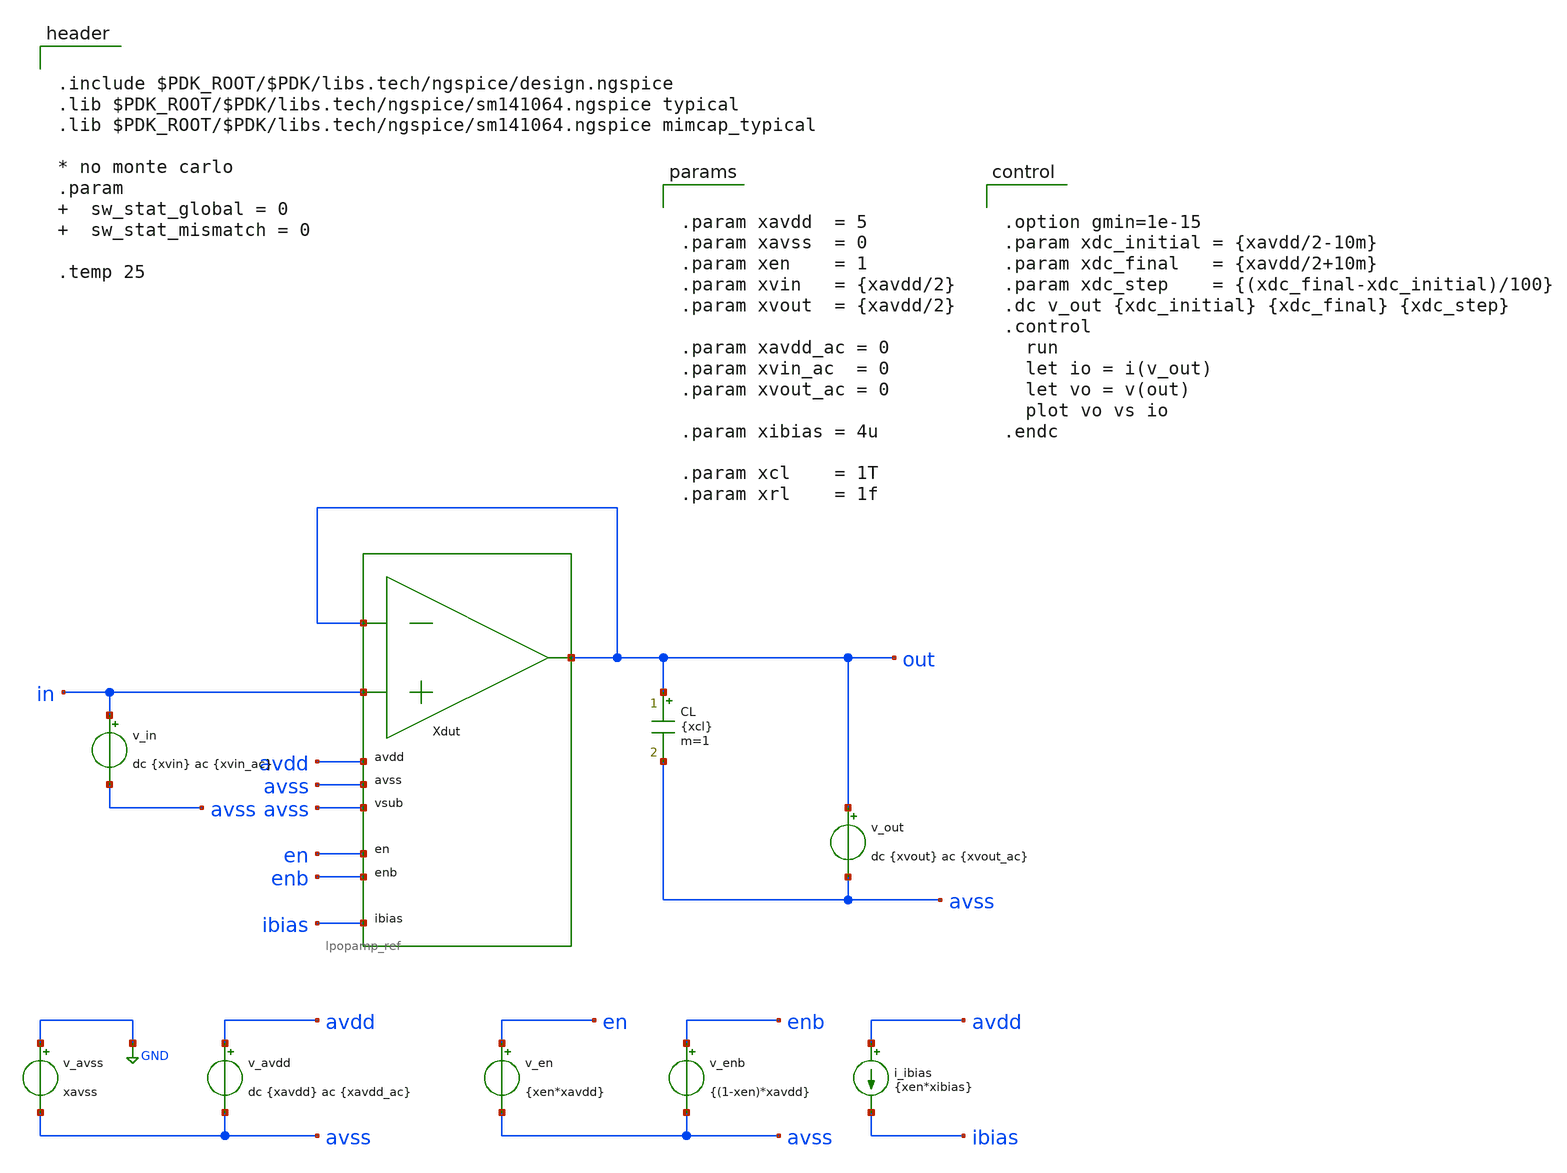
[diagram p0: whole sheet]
** sch_path: xschem/tb_lpopamp_buf_io.sch
**.subckt tb_lpopamp_buf_io
Xdut out in out avdd avss avss en enb ibias lpopamp_ref
v_avss GND avss xavss
v_avdd avdd avss dc {xavdd} ac {xavdd_ac}
v_in in avss dc {xvin} ac {xvin_ac}
v_en en avss {xen*xavdd}
v_enb enb avss {(1-xen)*xavdd}
i_ibias avdd ibias {xen*xibias}
CL out avss {xcl} m=1
v_out out avss dc {xvout} ac {xvout_ac}
**** begin user architecture code


.include $PDK_ROOT/$PDK/libs.tech/ngspice/design.ngspice
.lib $PDK_ROOT/$PDK/libs.tech/ngspice/sm141064.ngspice typical
.lib $PDK_ROOT/$PDK/libs.tech/ngspice/sm141064.ngspice mimcap_typical

* no monte carlo
.param   sw_stat_global = 0   sw_stat_mismatch = 0

.temp 25




.option gmin=1e-15
.param xdc_initial = {xavdd/2-10m}
.param xdc_final   = {xavdd/2+10m}
.param xdc_step    = {(xdc_final-xdc_initial)/100}
.dc v_out {xdc_initial} {xdc_final} {xdc_step}
.control
  run
  let io = i(v_out)
  let vo = v(out)
  plot vo vs io
.endc




.param xavdd  = 5
.param xavss  = 0
.param xen    = 1
.param xvin   = {xavdd/2}
.param xvout  = {xavdd/2}

.param xavdd_ac = 0
.param xvin_ac  = 0
.param xvout_ac = 0

.param xibias = 4u

.param xcl    = 1T
.param xrl    = 1f


**** end user architecture code
**.ends
.GLOBAL GND
.end
